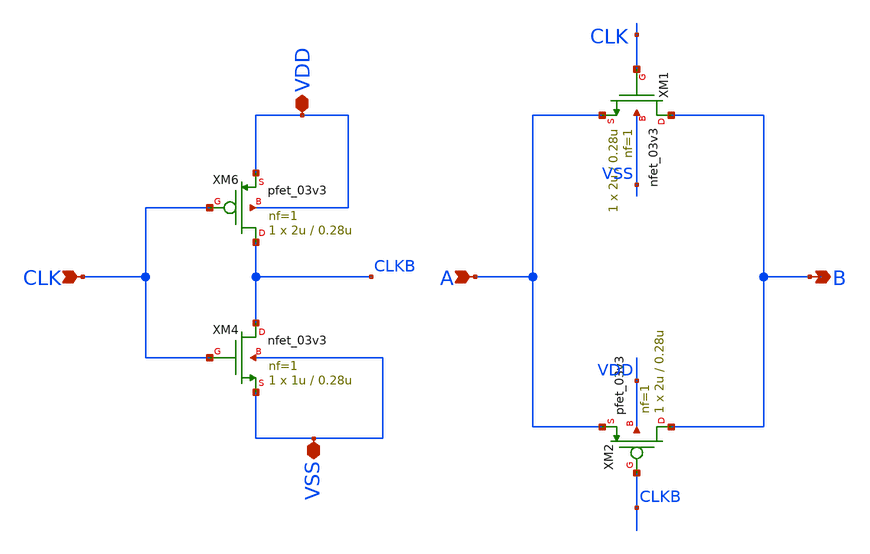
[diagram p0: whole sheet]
** sch_path: AWG_OUTPUT_AND_MUX_PAKISTAN_05/xschem/TGATE_PGA.sch
**.subckt TGATE_PGA VDD VSS B CLK A
*.iopin VDD
*.iopin VSS
*.opin B
*.ipin CLK
*.ipin A
XM4 CLKB CLK VSS VSS nfet_03v3 L=0.28u W=1u nf=1 ad='int((nf+1)/2) * W/nf * 0.18u' as='int((nf+2)/2) * W/nf * 0.18u'
+ pd='2*int((nf+1)/2) * (W/nf + 0.18u)' ps='2*int((nf+2)/2) * (W/nf + 0.18u)' nrd='0.18u / W' nrs='0.18u / W'
+ sa=0 sb=0 sd=0 m=1
XM6 CLKB CLK VDD VDD pfet_03v3 L=0.28u W=2u nf=1 ad='int((nf+1)/2) * W/nf * 0.18u' as='int((nf+2)/2) * W/nf * 0.18u'
+ pd='2*int((nf+1)/2) * (W/nf + 0.18u)' ps='2*int((nf+2)/2) * (W/nf + 0.18u)' nrd='0.18u / W' nrs='0.18u / W'
+ sa=0 sb=0 sd=0 m=1
XM1 B CLK A VSS nfet_03v3 L=0.28u W=2u nf=1 ad='int((nf+1)/2) * W/nf * 0.18u' as='int((nf+2)/2) * W/nf * 0.18u'
+ pd='2*int((nf+1)/2) * (W/nf + 0.18u)' ps='2*int((nf+2)/2) * (W/nf + 0.18u)' nrd='0.18u / W' nrs='0.18u / W'
+ sa=0 sb=0 sd=0 m=1
XM2 B CLKB A VDD pfet_03v3 L=0.28u W=2u nf=1 ad='int((nf+1)/2) * W/nf * 0.18u' as='int((nf+2)/2) * W/nf * 0.18u'
+ pd='2*int((nf+1)/2) * (W/nf + 0.18u)' ps='2*int((nf+2)/2) * (W/nf + 0.18u)' nrd='0.18u / W' nrs='0.18u / W'
+ sa=0 sb=0 sd=0 m=1
**.ends
.end
